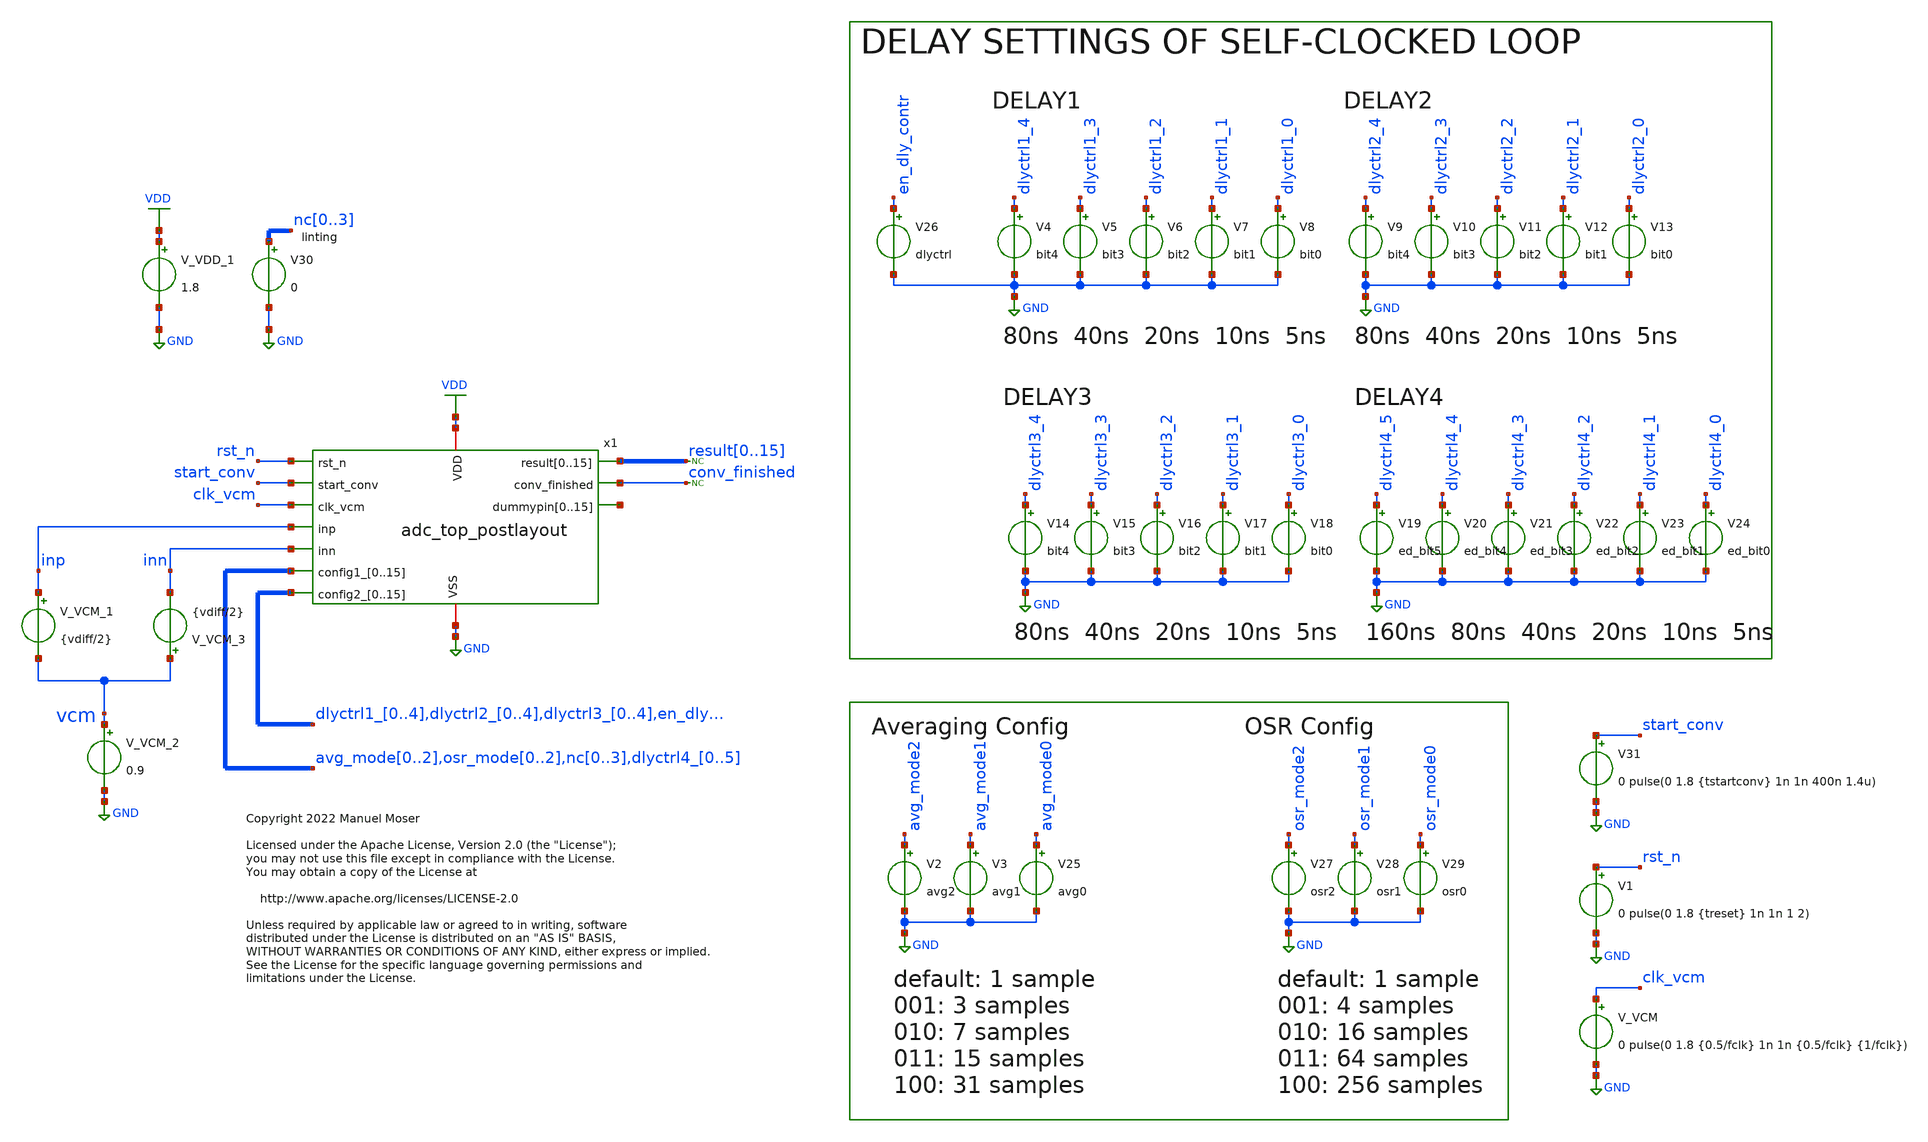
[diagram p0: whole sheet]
** sch_path: xschem/adc_top_postlayout_tb.sch
* Copyright 2022 Manuel Moser
* Licensed under the Apache License, Version 2.0 (the "License");
**.subckt adc_top_postlayout_tb
V_VDD_1 VDD GND 1.8
V_VCM_2 vcm GND 0.9
* noconn result[0..15]
* noconn conv_finished
V_VCM_1 inp vcm {vdiff/2}
V_VCM_3 vcm inn {vdiff/2}
V_VCM clk_vcm GND 0 pulse(0 1.8 {0.5/fclk} 1n 1n {0.5/fclk} {1/fclk})
V1 rst_n GND 0 pulse(0 1.8 {treset} 1n 1n 1 2)
V31 start_conv GND 0 pulse(0 1.8 {tstartconv} 1n 1n 400n 1.4u)
V4 dlyctrl1_4 GND bit4
V5 dlyctrl1_3 GND bit3
V6 dlyctrl1_2 GND bit2
V7 dlyctrl1_1 GND bit1
V8 dlyctrl1_0 GND bit0
V2 avg_mode2 GND avg2
V3 avg_mode1 GND avg1
V25 avg_mode0 GND avg0
V9 dlyctrl2_4 GND bit4
V10 dlyctrl2_3 GND bit3
V11 dlyctrl2_2 GND bit2
V12 dlyctrl2_1 GND bit1
V13 dlyctrl2_0 GND bit0
V14 dlyctrl3_4 GND bit4
V15 dlyctrl3_3 GND bit3
V16 dlyctrl3_2 GND bit2
V17 dlyctrl3_1 GND bit1
V18 dlyctrl3_0 GND bit0
V19 dlyctrl4_5 GND ed_bit5
V20 dlyctrl4_4 GND ed_bit4
V21 dlyctrl4_3 GND ed_bit3
V22 dlyctrl4_2 GND ed_bit2
V23 dlyctrl4_1 GND ed_bit1
V24 dlyctrl4_0 GND ed_bit0
V26 en_dly_contr GND dlyctrl
V27 osr_mode2 GND osr2
V28 osr_mode1 GND osr1
V29 osr_mode0 GND osr0
V30 nc0 GND 0
x1 result0 result1 result2 result3 result4 result5 result6 result7 result8 result9 result10 result11
+ result12 result13 result14 result15 VDD GND conv_finished rst_n start_conv clk_vcm inp inn avg_mode0
+ avg_mode1 avg_mode2 osr_mode0 osr_mode1 osr_mode2 nc0 nc1 nc2 nc3 dlyctrl4_0 dlyctrl4_1 dlyctrl4_2 dlyctrl4_3
+ dlyctrl4_4 dlyctrl4_5 dlyctrl1_0 dlyctrl1_1 dlyctrl1_2 dlyctrl1_3 dlyctrl1_4 dlyctrl2_0 dlyctrl2_1 dlyctrl2_2
+ dlyctrl2_3 dlyctrl2_4 dlyctrl3_0 dlyctrl3_1 dlyctrl3_2 dlyctrl3_3 dlyctrl3_4 en_dly_contr net1[15] net1[14]
+ net1[13] net1[12] net1[11] net1[10] net1[9] net1[8] net1[7] net1[6] net1[5] net1[4] net1[3] net1[2] net1[1]
+ net1[0] adc_top_postlayout
**** begin user architecture code


****************
* True mixed signal? (xspice) or analog? (spice)
****************
.options method=gear
*.include /foss/designs/SKY130_SAR-ADC/openlane/spice/adc_core_digital.spice
*.include /foss/designs/SKY130_SAR-ADC/verilog/xspice/adc_core_digital.xspice

*.include /foss/designs/SKY130_SAR-ADC/openlane/spice/adc_clkgen_with_edgedetect.spice
*.include /foss/designs/SKY130_SAR-ADC/verilog/xspice/adc_clkgen_with_edgedetect.xspice

.include ../../spice/adc_top.gds.postlayout.spice

* mind the order: include AFTER XSPICE FILES
*.include /foss/pdk/sky130A/libs.ref/sky130_fd_sc_hd/spice/sky130_fd_sc_hd.spice


****************
* Misc
****************
.param fclk=32768
.param treset=100n
.param tstartconv=500n
.param vdiff=200m

****************
* Delay Config
****************
.param dlyctrl = 1.8

* delay 1-3
.param bit0 = 0
.param bit1 = 1.8
.param bit2 = 0
.param bit3 = 0
.param bit4 = 0

* edgedetect pulse
.param ed_bit0 = 0
.param ed_bit1 = 0
.param ed_bit2 = 1.8
.param ed_bit3 = 1.8
.param ed_bit4 = 0
.param ed_bit5 = 0

****************
* Averaging Config
****************
.param avg0 = 0
.param avg1 = 0
.param avg2 = 0

****************
* OSR Config
****************
.param osr0 = 0
.param osr1 = 0
.param osr2 = 0


.save all
.control
set num_threads=11
tran 250p 3.2u
plot inp inn rst_n start_conv conv_finished
plot start_conv x1.clk_dig x1.clk_comp
plot x1.pctop x1.nctop x1.comparator_result
plot x1.pctop-x1.nctop

let k = length(time) - 1

* Print the result vector at the end of tran
print result15[k] result14[k] result13[k] result12[k] result11[k] result10[k] result9[k] result8[k]
+ result7[k] result6[k] result5[k] result4[k] result3[k] result2[k] result1[k] result0[k]
* Print the result diff-voltage at the end of tran
print
+ ((result15[k]*2048+result14[k]*1024+result13[k]*512+result12[k]*256+result11[k]*128+result10[k]*64+result9[k]*32+result8[k]*16+result7[k]*8+result6[k]*4+result5[k]*2+result4[k]*1+result3[k]*0.5+result2[k]*0.25+result1[k]*0.125+result0[k]*0.0625)-2048*1.8)/2048
.endc



** opencircuitdesign pdks install
.lib $::SKYWATER_MODELS/sky130.lib.spice tt


**** end user architecture code
**.ends
.GLOBAL VDD
.GLOBAL GND
.end
